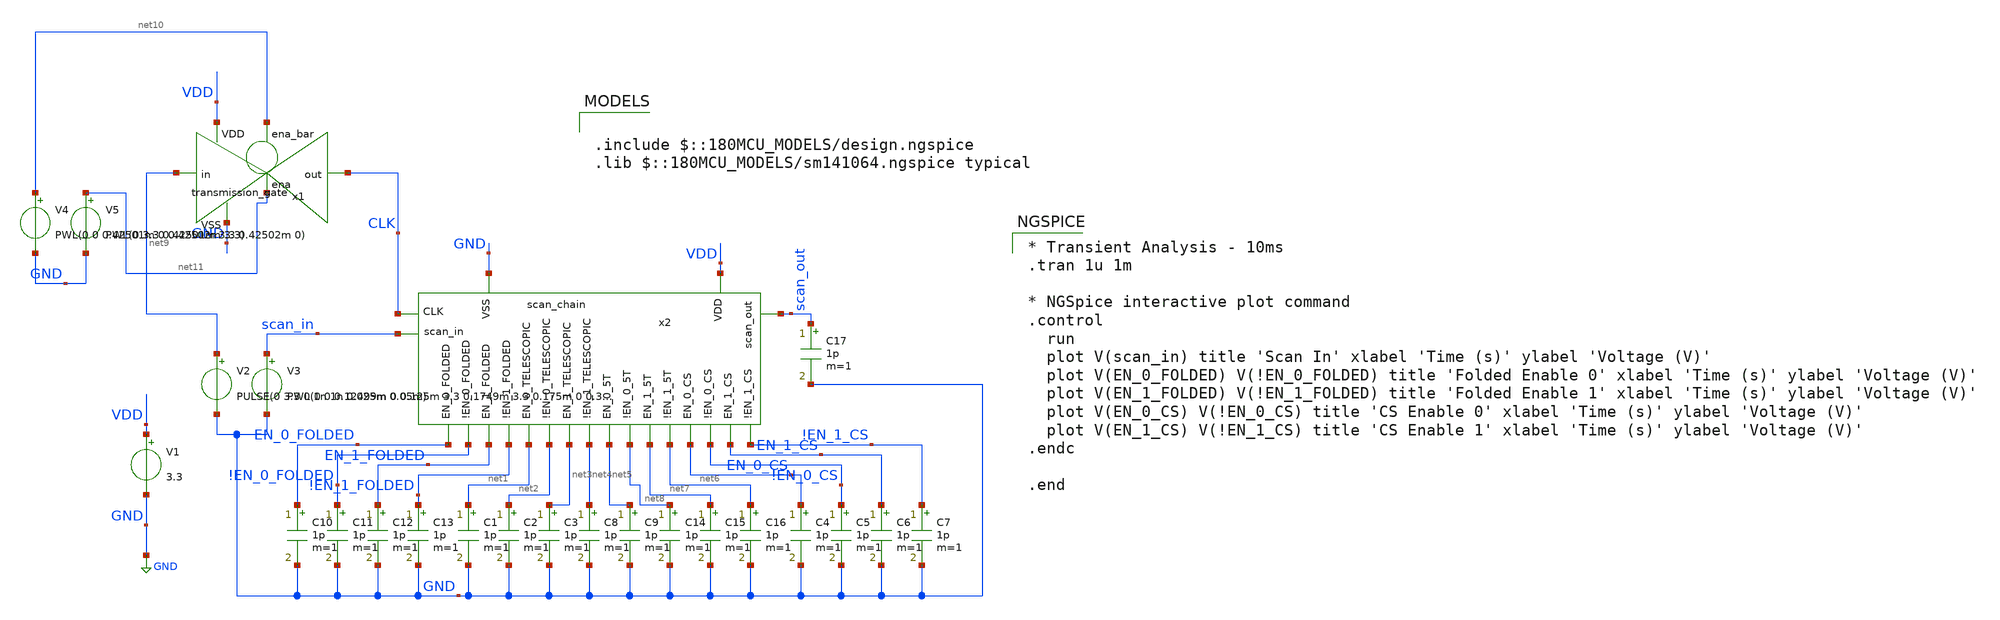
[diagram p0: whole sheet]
** sch_path: designs/libs/core_digital/tb/TB_scan_chain.sch
**.subckt TB_scan_chain
V1 VDD GND 3.3
C1 net1 GND 1p m=1
C2 net2 GND 1p m=1
C3 net3 GND 1p m=1
C8 net4 GND 1p m=1
C10 EN_0_FOLDED GND 1p m=1
C11 !EN_0_FOLDED GND 1p m=1
C12 EN_1_FOLDED GND 1p m=1
C13 !EN_1_FOLDED GND 1p m=1
C4 EN_0_CS GND 1p m=1
C5 !EN_0_CS GND 1p m=1
C6 EN_1_CS GND 1p m=1
C7 !EN_1_CS GND 1p m=1
C9 net5 GND 1p m=1
C14 net8 GND 1p m=1
C15 net7 GND 1p m=1
C16 net6 GND 1p m=1
C17 scan_out GND 1p m=1
V2 net9 GND PULSE(0 3.3 0 1n 1n 0.025m 0.05m)
V3 scan_in GND PWL(0 0 0.12499m 0 0.125m 3.3 0.1749m 3.3 0.175m 0 0.34999m 0 0.35m 3.3 0.499999m 3.3
+ 0.5m 0)
x2 VDD scan_out net7 net5 EN_0_CS EN_1_CS net1 EN_1_FOLDED EN_0_FOLDED net3 scan_in !EN_1_FOLDED
+ !EN_1_CS net2 !EN_0_CS net6 net8 net4 !EN_0_FOLDED CLK GND scan_chain
x1 net10 VDD CLK net9 GND net11 transmission_gate
V4 net10 GND PWL(0 0 0.42501m 0 0.42502m 3.3)
V5 net11 GND PWL(0 3.3 0.42501m 3.3 0.42502m 0)
**** begin user architecture code

.include $::180MCU_MODELS/design.ngspice
.lib $::180MCU_MODELS/sm141064.ngspice typical

 * Transient Analysis - 10ms
.tran 1u 1m

* NGSpice interactive plot command
.control
  run
  plot V(scan_in) title 'Scan In' xlabel 'Time (s)' ylabel 'Voltage (V)'
  plot V(EN_0_FOLDED) V(!EN_0_FOLDED) title 'Folded Enable 0' xlabel 'Time (s)' ylabel 'Voltage (V)'
  plot V(EN_1_FOLDED) V(!EN_1_FOLDED) title 'Folded Enable 1' xlabel 'Time (s)' ylabel 'Voltage (V)'
  plot V(EN_0_CS) V(!EN_0_CS) title 'CS Enable 0' xlabel 'Time (s)' ylabel 'Voltage (V)'
  plot V(EN_1_CS) V(!EN_1_CS) title 'CS Enable 1' xlabel 'Time (s)' ylabel 'Voltage (V)'
.endc

.end
**** end user architecture code
**.ends
.GLOBAL GND
.end
